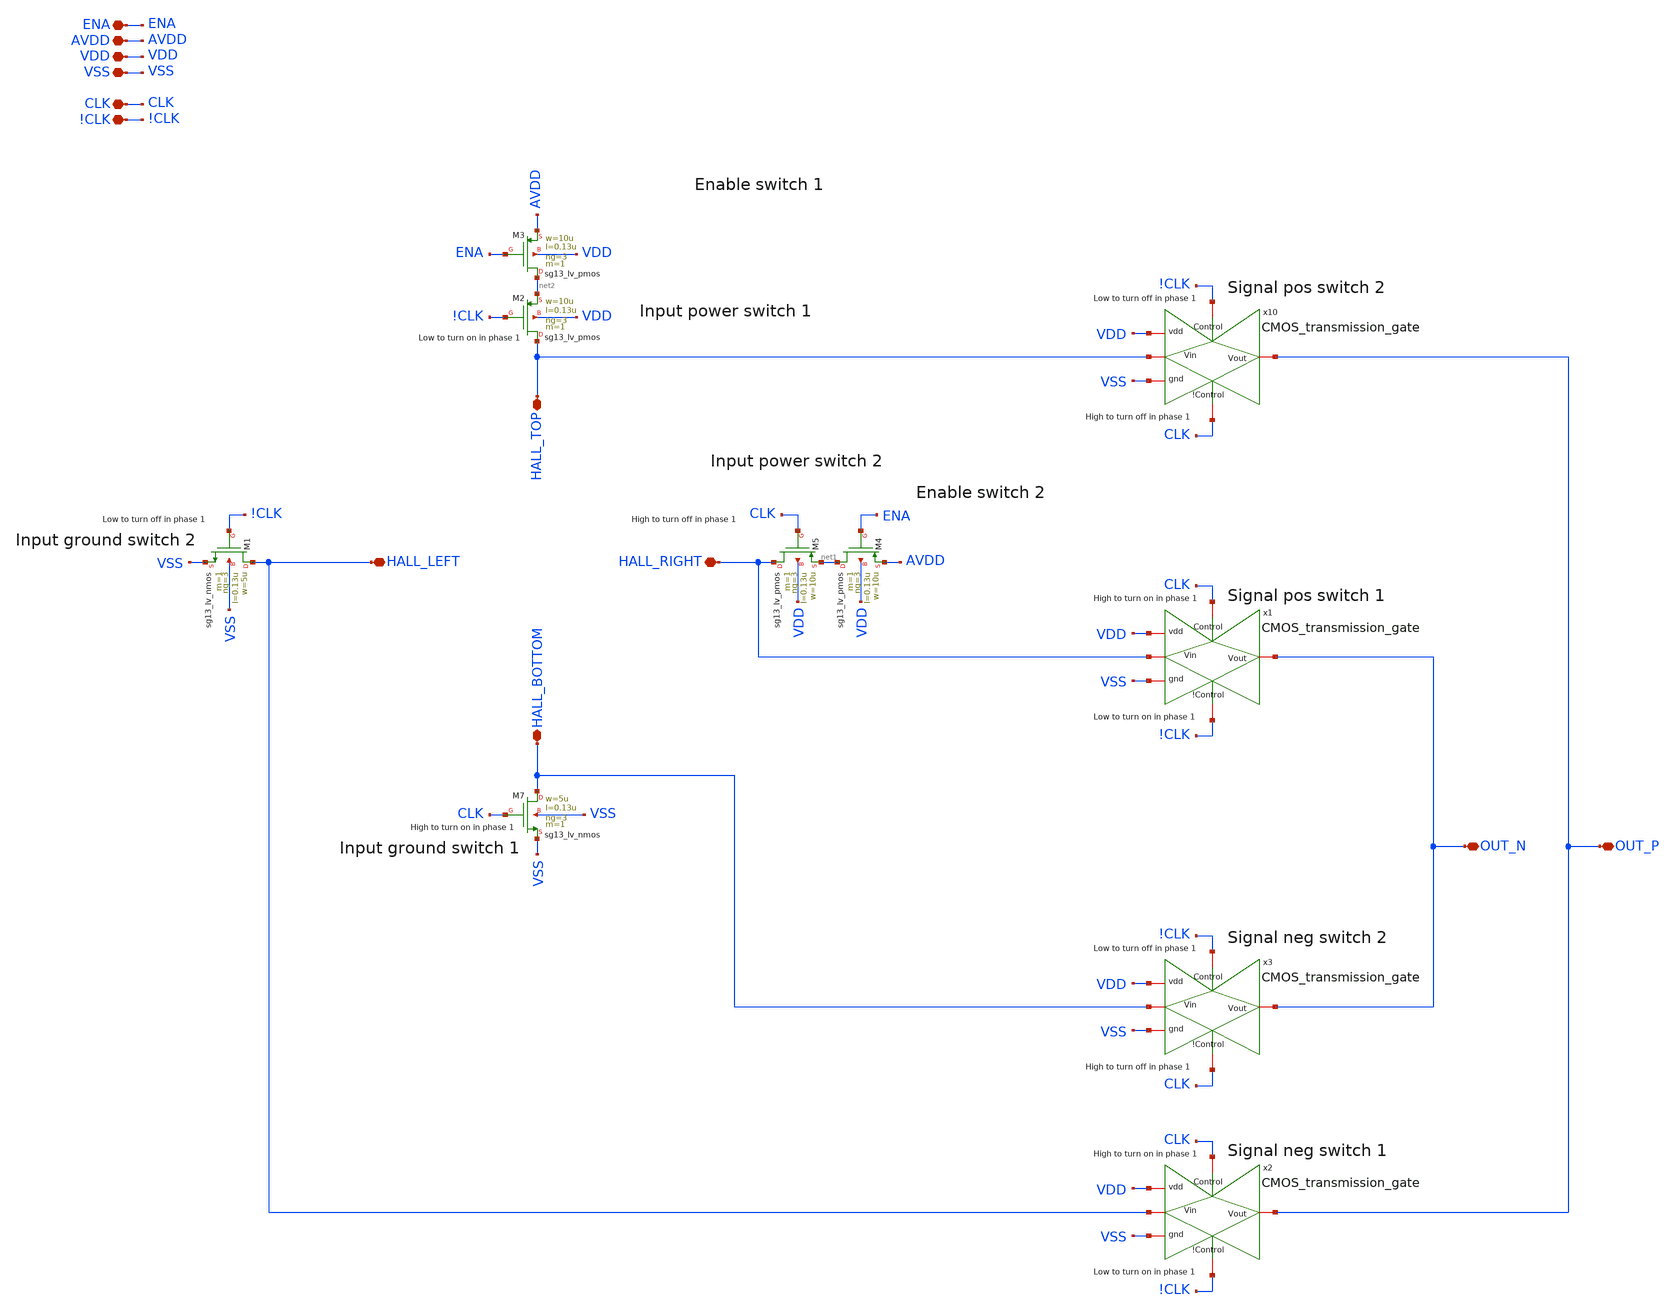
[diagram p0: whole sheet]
** sch_path: xschem/Rotator.sch
**.subckt Rotator HALL_TOP HALL_RIGHT HALL_LEFT HALL_BOTTOM OUT_P OUT_N VDD VSS CLK !CLK AVDD ENA
*.iopin HALL_TOP
*.iopin HALL_RIGHT
*.iopin HALL_LEFT
*.iopin HALL_BOTTOM
*.iopin OUT_P
*.iopin OUT_N
*.iopin VDD
*.iopin VSS
*.iopin CLK
*.iopin !CLK
*.iopin AVDD
*.iopin ENA
x10 CLK VDD HALL_TOP OUT_P VSS !CLK CMOS_transmission_gate
XM7 HALL_BOTTOM CLK VSS VSS sg13_lv_nmos w=5u l=0.13u ng=3 m=1 mm_ok=1
XM1 HALL_LEFT !CLK VSS VSS sg13_lv_nmos w=5u l=0.13u ng=3 m=1 mm_ok=1
XM5 HALL_RIGHT CLK net1 VDD sg13_lv_pmos w=10u l=0.13u ng=3 m=1 mm_ok=1
XM2 HALL_TOP !CLK net2 VDD sg13_lv_pmos w=10u l=0.13u ng=3 m=1 mm_ok=1
x1 !CLK VDD HALL_RIGHT OUT_N VSS CLK CMOS_transmission_gate
x2 !CLK VDD HALL_LEFT OUT_P VSS CLK CMOS_transmission_gate
x3 CLK VDD HALL_BOTTOM OUT_N VSS !CLK CMOS_transmission_gate
XM3 net2 ENA AVDD VDD sg13_lv_pmos w=10u l=0.13u ng=3 m=1 mm_ok=1
XM4 net1 ENA AVDD VDD sg13_lv_pmos w=10u l=0.13u ng=3 m=1 mm_ok=1
**.ends

* expanding   symbol:  /headless/eda/Hall_Xschem_Logic/CMOS_transmission_gate.sym # of pins=6
** sym_path: xschem/CMOS_transmission_gate.sym
** sch_path: xschem/CMOS_transmission_gate.sch
.subckt CMOS_transmission_gate !Control vdd Vin Vout gnd Control
*.iopin Vout
*.iopin Vin
*.iopin !Control
*.iopin Control
*.iopin gnd
*.iopin vdd
XM1 Vin Control Vout gnd sg13_lv_nmos w=0.5u l=0.13u ng=1 m=1 mm_ok=1
XM2 Vin !Control Vout vdd sg13_lv_pmos w=1u l=0.13u ng=1 m=1 mm_ok=1
.ends

.end
